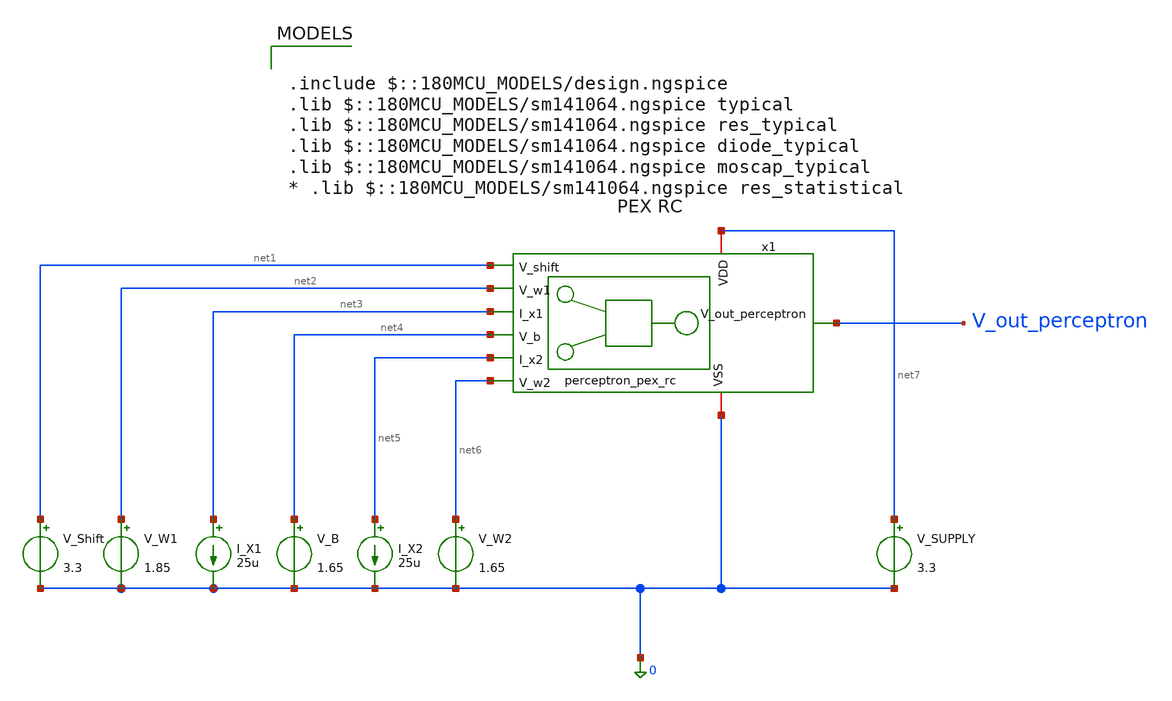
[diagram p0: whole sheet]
** sch_path: pex/xschem/tb_demo_perceptron_rc.sch
**.subckt tb_demo_perceptron_rc
V_SUPPLY net7 0 3.3
I_X1 net3 0 25u
I_X2 net5 0 25u
V_W1 net2 0 1.85
V_W2 net6 0 1.65
V_B net4 0 1.65
V_Shift net1 0 3.3
x1 net7 net1 net2 net3 V_out_perceptron net4 net5 net6 0 perceptron_pex_rc
**** begin user architecture code


.control
  op
  print all
  print v(V_out_perceptron)
.endc



.include $::180MCU_MODELS/design.ngspice
.lib $::180MCU_MODELS/sm141064.ngspice typical
.lib $::180MCU_MODELS/sm141064.ngspice res_typical
.lib $::180MCU_MODELS/sm141064.ngspice diode_typical
.lib $::180MCU_MODELS/sm141064.ngspice moscap_typical
* .lib $::180MCU_MODELS/sm141064.ngspice res_statistical

**** end user architecture code
**.ends

* expanding   symbol:  analog-perceptron-gf180mcu/pex/xschem/perceptron_pex_rc.sym # of pins=9
** sym_path: pex/xschem/perceptron_pex_rc.sym
.include /foss/designs/analog-perceptron-gf180mcu/pex/out/pex/perceptron_pex_rc.spice
.end
